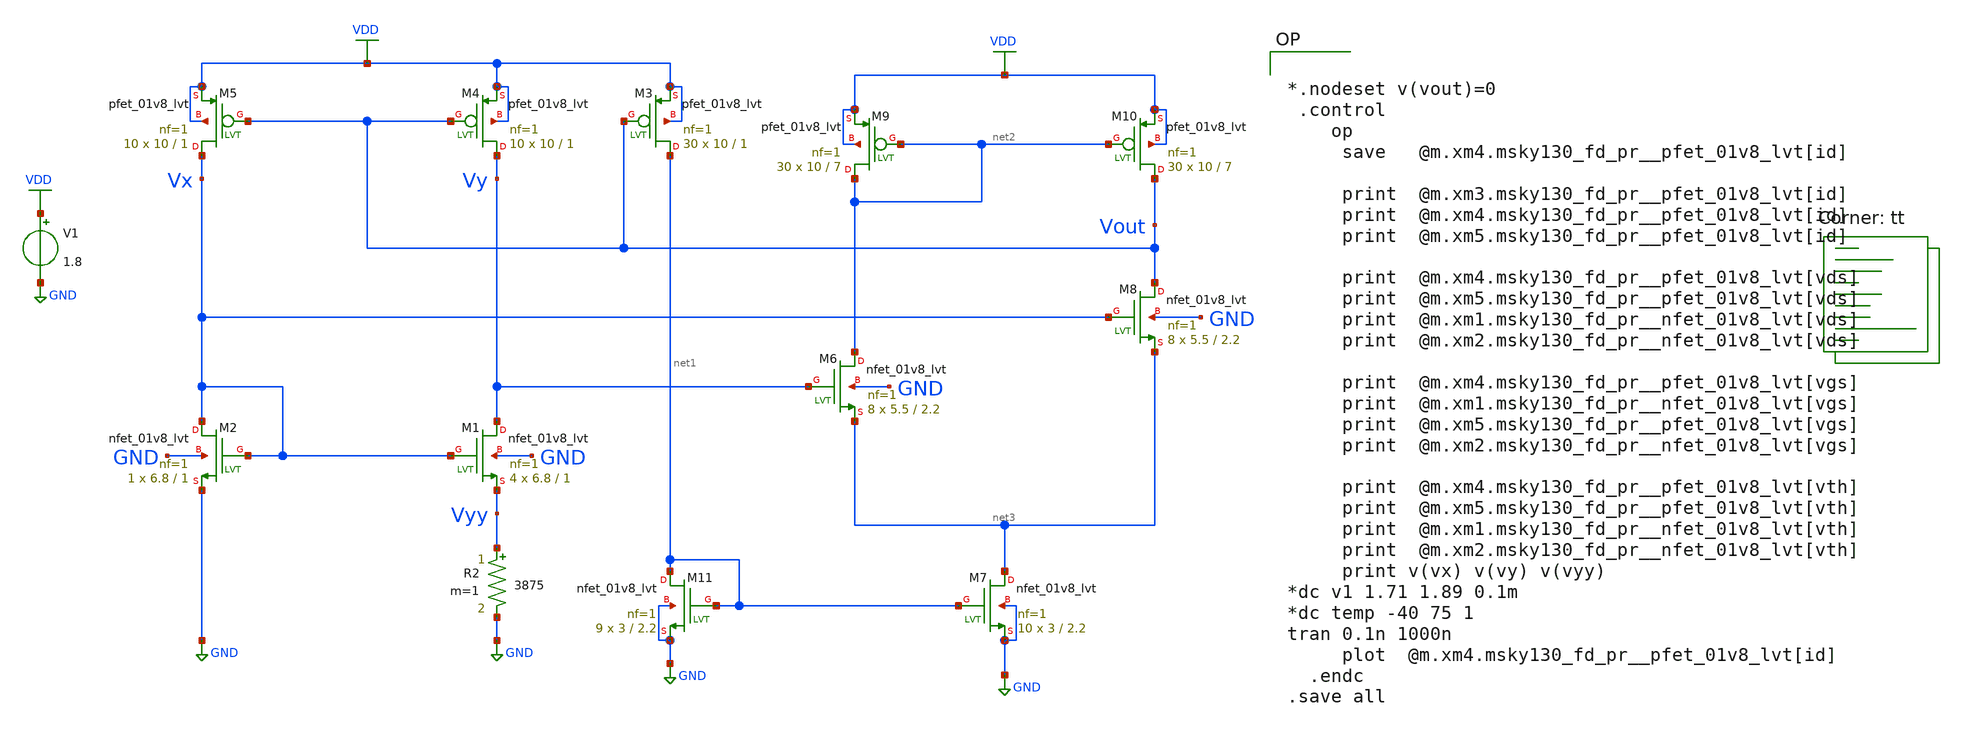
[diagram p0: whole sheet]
** sch_path: pll/lc_vco_lib_Hossam_Tarek/biasing_cct/xschem/constant_GM2_2.sch
**.subckt constant_GM2_2
XM1 Vy Vx Vyy GND sky130_fd_pr__nfet_01v8_lvt L=1 W=6.8 nf=1 ad='int((nf+1)/2) * W/nf * 0.29' as='int((nf+2)/2) * W/nf * 0.29'
+ pd='2*int((nf+1)/2) * (W/nf + 0.29)' ps='2*int((nf+2)/2) * (W/nf + 0.29)' nrd='0.29 / W' nrs='0.29 / W'
+ sa=0 sb=0 sd=0 mult=4 m=4
XM2 Vx Vx GND GND sky130_fd_pr__nfet_01v8_lvt L=1 W=6.8 nf=1 ad='int((nf+1)/2) * W/nf * 0.29' as='int((nf+2)/2) * W/nf * 0.29'
+ pd='2*int((nf+1)/2) * (W/nf + 0.29)' ps='2*int((nf+2)/2) * (W/nf + 0.29)' nrd='0.29 / W' nrs='0.29 / W'
+ sa=0 sb=0 sd=0 mult=1 m=1
XM4 Vy Vout VDD VDD sky130_fd_pr__pfet_01v8_lvt L=1 W=10 nf=1 ad='int((nf+1)/2) * W/nf * 0.29' as='int((nf+2)/2) * W/nf * 0.29'
+ pd='2*int((nf+1)/2) * (W/nf + 0.29)' ps='2*int((nf+2)/2) * (W/nf + 0.29)' nrd='0.29 / W' nrs='0.29 / W'
+ sa=0 sb=0 sd=0 mult=10 m=10
XM5 Vx Vout VDD VDD sky130_fd_pr__pfet_01v8_lvt L=1 W=10 nf=1 ad='int((nf+1)/2) * W/nf * 0.29' as='int((nf+2)/2) * W/nf * 0.29'
+ pd='2*int((nf+1)/2) * (W/nf + 0.29)' ps='2*int((nf+2)/2) * (W/nf + 0.29)' nrd='0.29 / W' nrs='0.29 / W'
+ sa=0 sb=0 sd=0 mult=10 m=10
R2 Vyy GND 3875 m=1
V1 VDD GND 1.8
XM6 net2 Vy net3 GND sky130_fd_pr__nfet_01v8_lvt L=2.2 W=5.5 nf=1 ad='int((nf+1)/2) * W/nf * 0.29' as='int((nf+2)/2) * W/nf * 0.29'
+ pd='2*int((nf+1)/2) * (W/nf + 0.29)' ps='2*int((nf+2)/2) * (W/nf + 0.29)' nrd='0.29 / W' nrs='0.29 / W'
+ sa=0 sb=0 sd=0 mult=8 m=8
XM7 net3 net1 GND GND sky130_fd_pr__nfet_01v8_lvt L=2.2 W=3 nf=1 ad='int((nf+1)/2) * W/nf * 0.29' as='int((nf+2)/2) * W/nf * 0.29'
+ pd='2*int((nf+1)/2) * (W/nf + 0.29)' ps='2*int((nf+2)/2) * (W/nf + 0.29)' nrd='0.29 / W' nrs='0.29 / W'
+ sa=0 sb=0 sd=0 mult=10 m=10
XM8 Vout Vx net3 GND sky130_fd_pr__nfet_01v8_lvt L=2.2 W=5.5 nf=1 ad='int((nf+1)/2) * W/nf * 0.29' as='int((nf+2)/2) * W/nf * 0.29'
+ pd='2*int((nf+1)/2) * (W/nf + 0.29)' ps='2*int((nf+2)/2) * (W/nf + 0.29)' nrd='0.29 / W' nrs='0.29 / W'
+ sa=0 sb=0 sd=0 mult=8 m=8
XM9 net2 net2 VDD VDD sky130_fd_pr__pfet_01v8_lvt L=7 W=10 nf=1 ad='int((nf+1)/2) * W/nf * 0.29' as='int((nf+2)/2) * W/nf * 0.29'
+ pd='2*int((nf+1)/2) * (W/nf + 0.29)' ps='2*int((nf+2)/2) * (W/nf + 0.29)' nrd='0.29 / W' nrs='0.29 / W'
+ sa=0 sb=0 sd=0 mult=30 m=30
XM10 Vout net2 VDD VDD sky130_fd_pr__pfet_01v8_lvt L=7 W=10 nf=1 ad='int((nf+1)/2) * W/nf * 0.29' as='int((nf+2)/2) * W/nf * 0.29'
+ pd='2*int((nf+1)/2) * (W/nf + 0.29)' ps='2*int((nf+2)/2) * (W/nf + 0.29)' nrd='0.29 / W' nrs='0.29 / W'
+ sa=0 sb=0 sd=0 mult=30 m=30
XM11 net1 net1 GND GND sky130_fd_pr__nfet_01v8_lvt L=2.2 W=3 nf=1 ad='int((nf+1)/2) * W/nf * 0.29' as='int((nf+2)/2) * W/nf * 0.29'
+ pd='2*int((nf+1)/2) * (W/nf + 0.29)' ps='2*int((nf+2)/2) * (W/nf + 0.29)' nrd='0.29 / W' nrs='0.29 / W'
+ sa=0 sb=0 sd=0 mult=9 m=9
XM3 net1 Vout VDD VDD sky130_fd_pr__pfet_01v8_lvt L=1 W=10 nf=1 ad='int((nf+1)/2) * W/nf * 0.29' as='int((nf+2)/2) * W/nf * 0.29'
+ pd='2*int((nf+1)/2) * (W/nf + 0.29)' ps='2*int((nf+2)/2) * (W/nf + 0.29)' nrd='0.29 / W' nrs='0.29 / W'
+ sa=0 sb=0 sd=0 mult=30 m=30
**** begin user architecture code


*.nodeset v(vout)=0
 .control
    op
     save   @m.xm4.msky130_fd_pr__pfet_01v8_lvt[id]

     print  @m.xm3.msky130_fd_pr__pfet_01v8_lvt[id]
     print  @m.xm4.msky130_fd_pr__pfet_01v8_lvt[id]
     print  @m.xm5.msky130_fd_pr__pfet_01v8_lvt[id]

     print  @m.xm4.msky130_fd_pr__pfet_01v8_lvt[vds]
     print  @m.xm5.msky130_fd_pr__pfet_01v8_lvt[vds]
     print  @m.xm1.msky130_fd_pr__nfet_01v8_lvt[vds]
     print  @m.xm2.msky130_fd_pr__nfet_01v8_lvt[vds]

     print  @m.xm4.msky130_fd_pr__pfet_01v8_lvt[vgs]
     print  @m.xm1.msky130_fd_pr__nfet_01v8_lvt[vgs]
     print  @m.xm5.msky130_fd_pr__pfet_01v8_lvt[vgs]
     print  @m.xm2.msky130_fd_pr__nfet_01v8_lvt[vgs]

     print  @m.xm4.msky130_fd_pr__pfet_01v8_lvt[vth]
     print  @m.xm5.msky130_fd_pr__pfet_01v8_lvt[vth]
     print  @m.xm1.msky130_fd_pr__nfet_01v8_lvt[vth]
     print  @m.xm2.msky130_fd_pr__nfet_01v8_lvt[vth]
     print v(vx) v(vy) v(vyy)
*dc v1 1.71 1.89 0.1m
*dc temp -40 75 1
tran 0.1n 1000n
     plot  @m.xm4.msky130_fd_pr__pfet_01v8_lvt[id]
  .endc
.save all

.lib $::SKYWATER_MODELS/sky130.lib.spice tt
**** end user architecture code
**.ends
.GLOBAL GND
.GLOBAL VDD
.end
